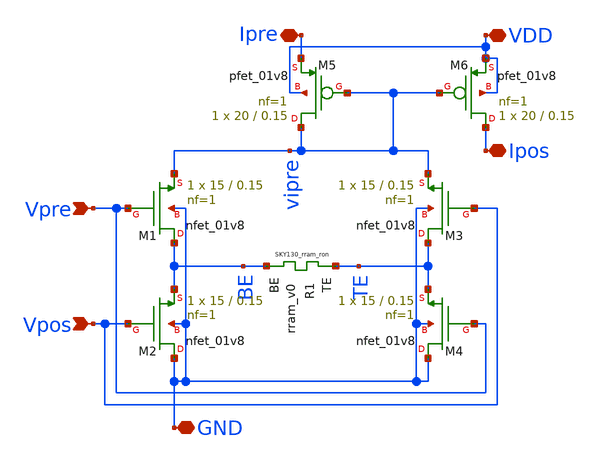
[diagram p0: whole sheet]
** sch_path: synapse/6T1R.sch
**.subckt 6T1R Vpre Vpos GND Ipos Ipre VDD
*.ipin Vpre
*.ipin Vpos
*.iopin GND
*.iopin Ipos
*.iopin Ipre
*.iopin VDD
XM1 BE Vpre vipre GND sky130_fd_pr__nfet_01v8 L=0.15 W=15 nf=1 ad='int((nf+1)/2) * W/nf * 0.29' as='int((nf+2)/2) * W/nf * 0.29'
+ pd='2*int((nf+1)/2) * (W/nf + 0.29)' ps='2*int((nf+2)/2) * (W/nf + 0.29)' nrd='0.29 / W' nrs='0.29 / W'
+ sa=0 sb=0 sd=0 mult=1 m=1
XR1 TE BE rram_v0
XM3 TE Vpos vipre GND sky130_fd_pr__nfet_01v8 L=0.15 W=15 nf=1 ad='int((nf+1)/2) * W/nf * 0.29' as='int((nf+2)/2) * W/nf * 0.29'
+ pd='2*int((nf+1)/2) * (W/nf + 0.29)' ps='2*int((nf+2)/2) * (W/nf + 0.29)' nrd='0.29 / W' nrs='0.29 / W'
+ sa=0 sb=0 sd=0 mult=1 m=1
XM6 Ipos vipre VDD VDD sky130_fd_pr__pfet_01v8 L=0.15 W=20 nf=1 ad='int((nf+1)/2) * W/nf * 0.29' as='int((nf+2)/2) * W/nf * 0.29'
+ pd='2*int((nf+1)/2) * (W/nf + 0.29)' ps='2*int((nf+2)/2) * (W/nf + 0.29)' nrd='0.29 / W' nrs='0.29 / W'
+ sa=0 sb=0 sd=0 mult=1 m=1
XM5 vipre vipre Ipre VDD sky130_fd_pr__pfet_01v8 L=0.15 W=20 nf=1 ad='int((nf+1)/2) * W/nf * 0.29' as='int((nf+2)/2) * W/nf * 0.29'
+ pd='2*int((nf+1)/2) * (W/nf + 0.29)' ps='2*int((nf+2)/2) * (W/nf + 0.29)' nrd='0.29 / W' nrs='0.29 / W'
+ sa=0 sb=0 sd=0 mult=1 m=1
XM2 GND Vpos BE GND sky130_fd_pr__nfet_01v8 L=0.15 W=15 nf=1 ad='int((nf+1)/2) * W/nf * 0.29' as='int((nf+2)/2) * W/nf * 0.29'
+ pd='2*int((nf+1)/2) * (W/nf + 0.29)' ps='2*int((nf+2)/2) * (W/nf + 0.29)' nrd='0.29 / W' nrs='0.29 / W'
+ sa=0 sb=0 sd=0 mult=1 m=1
XM4 GND Vpre TE GND sky130_fd_pr__nfet_01v8 L=0.15 W=15 nf=1 ad='int((nf+1)/2) * W/nf * 0.29' as='int((nf+2)/2) * W/nf * 0.29'
+ pd='2*int((nf+1)/2) * (W/nf + 0.29)' ps='2*int((nf+2)/2) * (W/nf + 0.29)' nrd='0.29 / W' nrs='0.29 / W'
+ sa=0 sb=0 sd=0 mult=1 m=1
**.ends
.end
